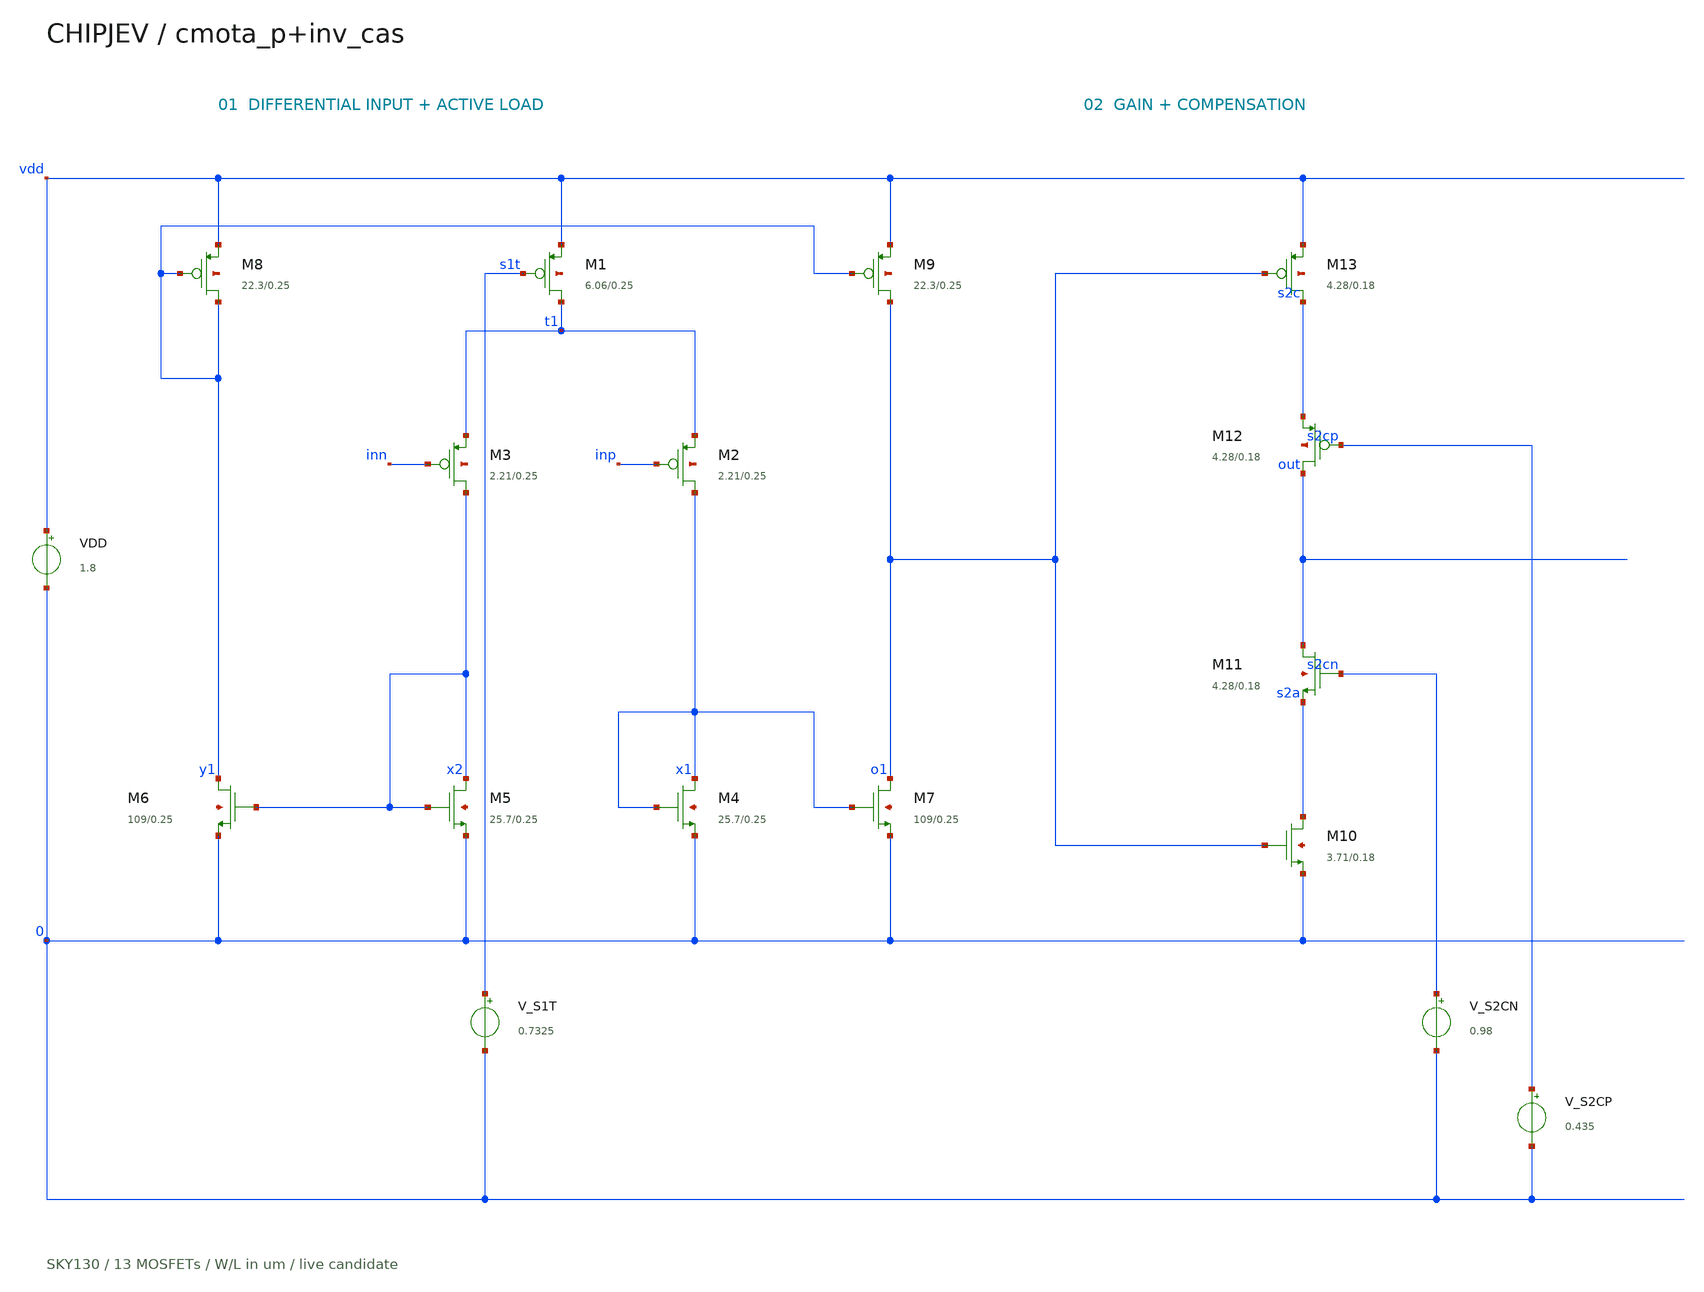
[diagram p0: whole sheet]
** sch_path: experiments/analog-layout/opamp-gain/circuit.sch
**.subckt circuit
VDD vdd 0 1.8
XM1 t1 s1t vdd vdd sky130_fd_pr__pfet_01v8 L=0.25 W=6.06 nf=1 ad=1.7574 as=1.7574 pd=12.7 ps=12.7
+ nrd=0.0478548 nrs=0.0478548 sa=0 sb=0 sd=0 mult=1 m=1
XM2 x1 inp t1 vdd sky130_fd_pr__pfet_01v8 L=0.25 W=2.21 nf=1 ad=0.6409 as=0.6409 pd=5 ps=5
+ nrd=0.131222 nrs=0.131222 sa=0 sb=0 sd=0 mult=1 m=1
XM3 x2 inn t1 vdd sky130_fd_pr__pfet_01v8 L=0.25 W=2.21 nf=1 ad=0.6409 as=0.6409 pd=5 ps=5
+ nrd=0.131222 nrs=0.131222 sa=0 sb=0 sd=0 mult=1 m=1
XM4 x1 x1 0 0 sky130_fd_pr__nfet_01v8 L=0.25 W=25.74 nf=1 ad=7.4646 as=7.4646 pd=52.06 ps=52.06
+ nrd=0.0112665 nrs=0.0112665 sa=0 sb=0 sd=0 mult=1 m=1
XM5 x2 x2 0 0 sky130_fd_pr__nfet_01v8 L=0.25 W=25.74 nf=1 ad=7.4646 as=7.4646 pd=52.06 ps=52.06
+ nrd=0.0112665 nrs=0.0112665 sa=0 sb=0 sd=0 mult=1 m=1
XM6 y1 x2 0 0 sky130_fd_pr__nfet_01v8 L=0.25 W=109.26 nf=3 ad=21.1236 as=21.1236 pd=146.84 ps=146.84
+ nrd=0.00265422 nrs=0.00265422 sa=0 sb=0 sd=0 mult=1 m=1
XM7 o1 x1 0 0 sky130_fd_pr__nfet_01v8 L=0.25 W=109.26 nf=3 ad=21.1236 as=21.1236 pd=146.84 ps=146.84
+ nrd=0.00265422 nrs=0.00265422 sa=0 sb=0 sd=0 mult=1 m=1
XM8 y1 y1 vdd vdd sky130_fd_pr__pfet_01v8 L=0.25 W=22.28 nf=1 ad=6.4612 as=6.4612 pd=45.14 ps=45.14
+ nrd=0.0130162 nrs=0.0130162 sa=0 sb=0 sd=0 mult=1 m=1
XM9 o1 y1 vdd vdd sky130_fd_pr__pfet_01v8 L=0.25 W=22.28 nf=1 ad=6.4612 as=6.4612 pd=45.14 ps=45.14
+ nrd=0.0130162 nrs=0.0130162 sa=0 sb=0 sd=0 mult=1 m=1
XM10 s2a o1 0 0 sky130_fd_pr__nfet_01v8 L=0.18 W=3.71 nf=1 ad=1.0759 as=1.0759 pd=8 ps=8
+ nrd=0.0781671 nrs=0.0781671 sa=0 sb=0 sd=0 mult=1 m=1
XM11 out s2cn s2a 0 sky130_fd_pr__nfet_01v8 L=0.18 W=4.28 nf=1 ad=1.2412 as=1.2412 pd=9.14 ps=9.14
+ nrd=0.067757 nrs=0.067757 sa=0 sb=0 sd=0 mult=1 m=1
XM12 out s2cp s2c vdd sky130_fd_pr__pfet_01v8 L=0.18 W=4.28 nf=1 ad=1.2412 as=1.2412 pd=9.14 ps=9.14
+ nrd=0.067757 nrs=0.067757 sa=0 sb=0 sd=0 mult=1 m=1
XM13 s2c o1 vdd vdd sky130_fd_pr__pfet_01v8 L=0.18 W=4.28 nf=1 ad=1.2412 as=1.2412 pd=9.14 ps=9.14
+ nrd=0.067757 nrs=0.067757 sa=0 sb=0 sd=0 mult=1 m=1
V_S1T s1t 0 0.7325
V_S2CN s2cn 0 0.98
V_S2CP s2cp 0 0.435
**.ends
.end
